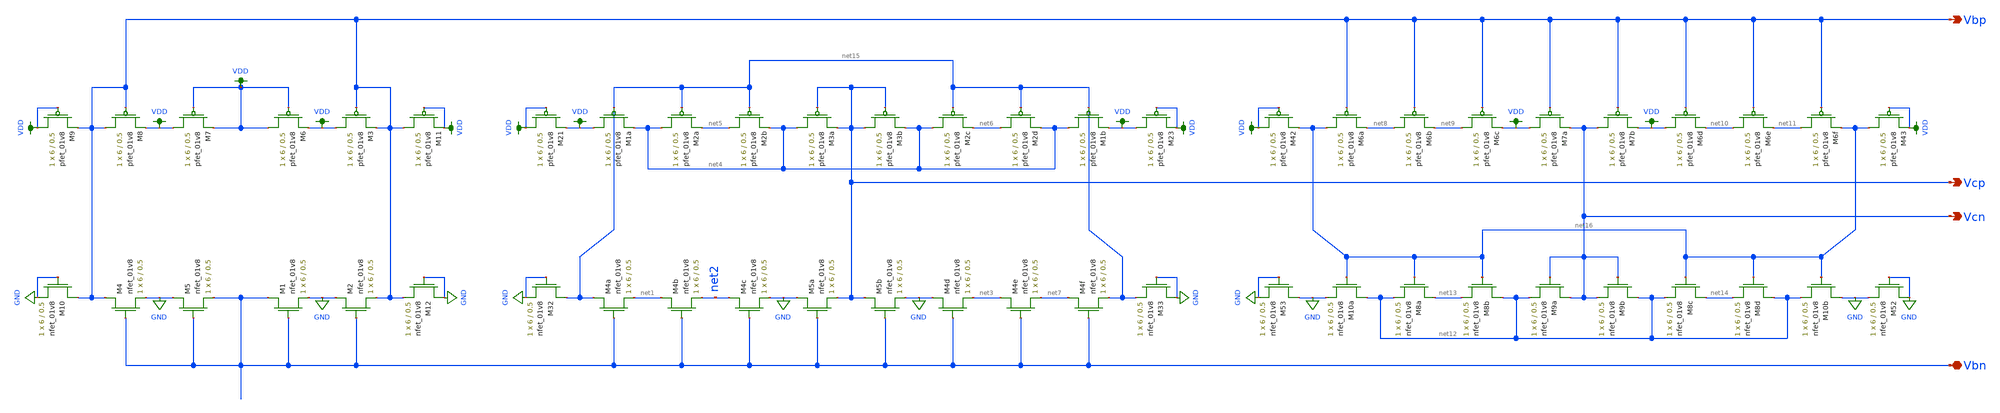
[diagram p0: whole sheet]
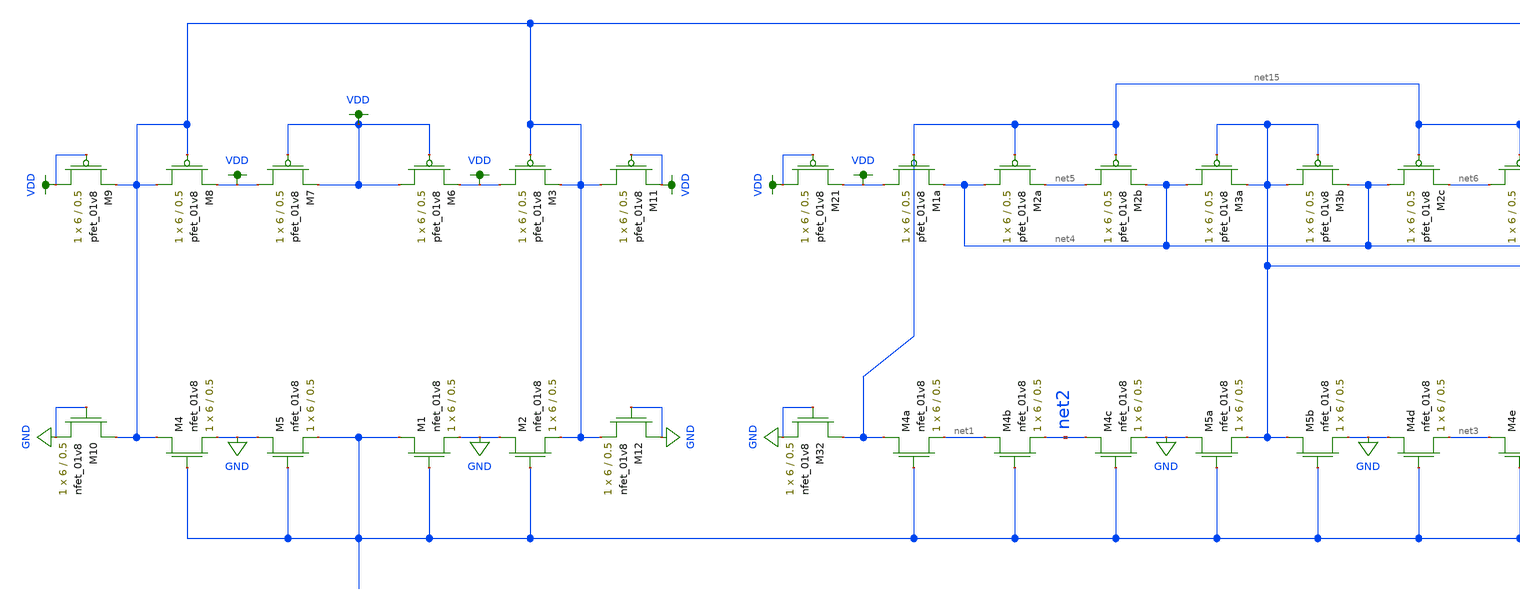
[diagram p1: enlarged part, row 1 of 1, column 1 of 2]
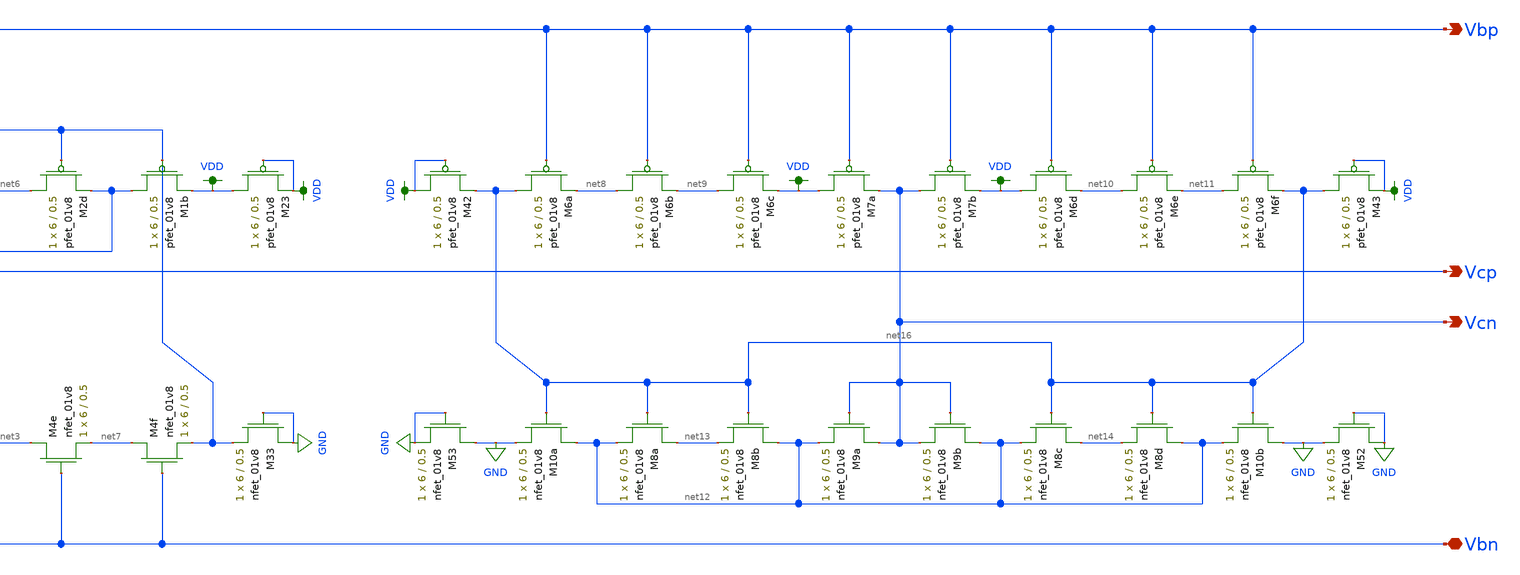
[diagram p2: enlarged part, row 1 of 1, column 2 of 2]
** sch_path: mini3/schem/bias_lvs.sch
**.subckt bias_lvs Vcn Vcp Vbp Vbn
*.opin Vcn
*.opin Vcp
*.opin Vbp
*.iopin Vbn
XM4a net15 Vbn net1 GND sky130_fd_pr__nfet_01v8 L=0.5 W=6 nf=1 ad='int((nf+1)/2) * W/nf * 0.29' as='int((nf+2)/2) * W/nf * 0.29'
+ pd='2*int((nf+1)/2) * (W/nf + 0.29)' ps='2*int((nf+2)/2) * (W/nf + 0.29)' nrd='0.29 / W' nrs='0.29 / W'
+ sa=0 sb=0 sd=0 mult=1 m=1
XM4b net1 Vbn net2 GND sky130_fd_pr__nfet_01v8 L=0.5 W=6 nf=1 ad='int((nf+1)/2) * W/nf * 0.29' as='int((nf+2)/2) * W/nf * 0.29'
+ pd='2*int((nf+1)/2) * (W/nf + 0.29)' ps='2*int((nf+2)/2) * (W/nf + 0.29)' nrd='0.29 / W' nrs='0.29 / W'
+ sa=0 sb=0 sd=0 mult=1 m=1
XM4c net2 Vbn GND GND sky130_fd_pr__nfet_01v8 L=0.5 W=6 nf=1 ad='int((nf+1)/2) * W/nf * 0.29' as='int((nf+2)/2) * W/nf * 0.29'
+ pd='2*int((nf+1)/2) * (W/nf + 0.29)' ps='2*int((nf+2)/2) * (W/nf + 0.29)' nrd='0.29 / W' nrs='0.29 / W'
+ sa=0 sb=0 sd=0 mult=1 m=1
XM5a GND Vbn Vcp GND sky130_fd_pr__nfet_01v8 L=0.5 W=6 nf=1 ad='int((nf+1)/2) * W/nf * 0.29' as='int((nf+2)/2) * W/nf * 0.29'
+ pd='2*int((nf+1)/2) * (W/nf + 0.29)' ps='2*int((nf+2)/2) * (W/nf + 0.29)' nrd='0.29 / W' nrs='0.29 / W'
+ sa=0 sb=0 sd=0 mult=1 m=1
XM5b Vcp Vbn GND GND sky130_fd_pr__nfet_01v8 L=0.5 W=6 nf=1 ad='int((nf+1)/2) * W/nf * 0.29' as='int((nf+2)/2) * W/nf * 0.29'
+ pd='2*int((nf+1)/2) * (W/nf + 0.29)' ps='2*int((nf+2)/2) * (W/nf + 0.29)' nrd='0.29 / W' nrs='0.29 / W'
+ sa=0 sb=0 sd=0 mult=1 m=1
XM4d GND Vbn net3 GND sky130_fd_pr__nfet_01v8 L=0.5 W=6 nf=1 ad='int((nf+1)/2) * W/nf * 0.29' as='int((nf+2)/2) * W/nf * 0.29'
+ pd='2*int((nf+1)/2) * (W/nf + 0.29)' ps='2*int((nf+2)/2) * (W/nf + 0.29)' nrd='0.29 / W' nrs='0.29 / W'
+ sa=0 sb=0 sd=0 mult=1 m=1
XM4e net3 Vbn net7 GND sky130_fd_pr__nfet_01v8 L=0.5 W=6 nf=1 ad='int((nf+1)/2) * W/nf * 0.29' as='int((nf+2)/2) * W/nf * 0.29'
+ pd='2*int((nf+1)/2) * (W/nf + 0.29)' ps='2*int((nf+2)/2) * (W/nf + 0.29)' nrd='0.29 / W' nrs='0.29 / W'
+ sa=0 sb=0 sd=0 mult=1 m=1
XM4f net7 Vbn net15 GND sky130_fd_pr__nfet_01v8 L=0.5 W=6 nf=1 ad='int((nf+1)/2) * W/nf * 0.29' as='int((nf+2)/2) * W/nf * 0.29'
+ pd='2*int((nf+1)/2) * (W/nf + 0.29)' ps='2*int((nf+2)/2) * (W/nf + 0.29)' nrd='0.29 / W' nrs='0.29 / W'
+ sa=0 sb=0 sd=0 mult=1 m=1
XM1a VDD net15 net4 VDD sky130_fd_pr__pfet_01v8 L=0.5 W=6 nf=1 ad='int((nf+1)/2) * W/nf * 0.29' as='int((nf+2)/2) * W/nf * 0.29'
+ pd='2*int((nf+1)/2) * (W/nf + 0.29)' ps='2*int((nf+2)/2) * (W/nf + 0.29)' nrd='0.29 / W' nrs='0.29 / W'
+ sa=0 sb=0 sd=0 mult=1 m=1
XM2a net4 net15 net5 VDD sky130_fd_pr__pfet_01v8 L=0.5 W=6 nf=1 ad='int((nf+1)/2) * W/nf * 0.29' as='int((nf+2)/2) * W/nf * 0.29'
+ pd='2*int((nf+1)/2) * (W/nf + 0.29)' ps='2*int((nf+2)/2) * (W/nf + 0.29)' nrd='0.29 / W' nrs='0.29 / W'
+ sa=0 sb=0 sd=0 mult=1 m=1
XM2b net5 net15 net4 VDD sky130_fd_pr__pfet_01v8 L=0.5 W=6 nf=1 ad='int((nf+1)/2) * W/nf * 0.29' as='int((nf+2)/2) * W/nf * 0.29'
+ pd='2*int((nf+1)/2) * (W/nf + 0.29)' ps='2*int((nf+2)/2) * (W/nf + 0.29)' nrd='0.29 / W' nrs='0.29 / W'
+ sa=0 sb=0 sd=0 mult=1 m=1
XM3a net4 Vcp Vcp VDD sky130_fd_pr__pfet_01v8 L=0.5 W=6 nf=1 ad='int((nf+1)/2) * W/nf * 0.29' as='int((nf+2)/2) * W/nf * 0.29'
+ pd='2*int((nf+1)/2) * (W/nf + 0.29)' ps='2*int((nf+2)/2) * (W/nf + 0.29)' nrd='0.29 / W' nrs='0.29 / W'
+ sa=0 sb=0 sd=0 mult=1 m=1
XM3b Vcp Vcp net4 VDD sky130_fd_pr__pfet_01v8 L=0.5 W=6 nf=1 ad='int((nf+1)/2) * W/nf * 0.29' as='int((nf+2)/2) * W/nf * 0.29'
+ pd='2*int((nf+1)/2) * (W/nf + 0.29)' ps='2*int((nf+2)/2) * (W/nf + 0.29)' nrd='0.29 / W' nrs='0.29 / W'
+ sa=0 sb=0 sd=0 mult=1 m=1
XM2c net4 net15 net6 VDD sky130_fd_pr__pfet_01v8 L=0.5 W=6 nf=1 ad='int((nf+1)/2) * W/nf * 0.29' as='int((nf+2)/2) * W/nf * 0.29'
+ pd='2*int((nf+1)/2) * (W/nf + 0.29)' ps='2*int((nf+2)/2) * (W/nf + 0.29)' nrd='0.29 / W' nrs='0.29 / W'
+ sa=0 sb=0 sd=0 mult=1 m=1
XM2d net6 net15 net4 VDD sky130_fd_pr__pfet_01v8 L=0.5 W=6 nf=1 ad='int((nf+1)/2) * W/nf * 0.29' as='int((nf+2)/2) * W/nf * 0.29'
+ pd='2*int((nf+1)/2) * (W/nf + 0.29)' ps='2*int((nf+2)/2) * (W/nf + 0.29)' nrd='0.29 / W' nrs='0.29 / W'
+ sa=0 sb=0 sd=0 mult=1 m=1
XM1b net4 net15 VDD VDD sky130_fd_pr__pfet_01v8 L=0.5 W=6 nf=1 ad='int((nf+1)/2) * W/nf * 0.29' as='int((nf+2)/2) * W/nf * 0.29'
+ pd='2*int((nf+1)/2) * (W/nf + 0.29)' ps='2*int((nf+2)/2) * (W/nf + 0.29)' nrd='0.29 / W' nrs='0.29 / W'
+ sa=0 sb=0 sd=0 mult=1 m=1
XM6a net16 Vbp net8 VDD sky130_fd_pr__pfet_01v8 L=0.5 W=6 nf=1 ad='int((nf+1)/2) * W/nf * 0.29' as='int((nf+2)/2) * W/nf * 0.29'
+ pd='2*int((nf+1)/2) * (W/nf + 0.29)' ps='2*int((nf+2)/2) * (W/nf + 0.29)' nrd='0.29 / W' nrs='0.29 / W'
+ sa=0 sb=0 sd=0 mult=1 m=1
XM6b net8 Vbp net9 VDD sky130_fd_pr__pfet_01v8 L=0.5 W=6 nf=1 ad='int((nf+1)/2) * W/nf * 0.29' as='int((nf+2)/2) * W/nf * 0.29'
+ pd='2*int((nf+1)/2) * (W/nf + 0.29)' ps='2*int((nf+2)/2) * (W/nf + 0.29)' nrd='0.29 / W' nrs='0.29 / W'
+ sa=0 sb=0 sd=0 mult=1 m=1
XM6c net9 Vbp VDD VDD sky130_fd_pr__pfet_01v8 L=0.5 W=6 nf=1 ad='int((nf+1)/2) * W/nf * 0.29' as='int((nf+2)/2) * W/nf * 0.29'
+ pd='2*int((nf+1)/2) * (W/nf + 0.29)' ps='2*int((nf+2)/2) * (W/nf + 0.29)' nrd='0.29 / W' nrs='0.29 / W'
+ sa=0 sb=0 sd=0 mult=1 m=1
XM7a VDD Vbp Vcn VDD sky130_fd_pr__pfet_01v8 L=0.5 W=6 nf=1 ad='int((nf+1)/2) * W/nf * 0.29' as='int((nf+2)/2) * W/nf * 0.29'
+ pd='2*int((nf+1)/2) * (W/nf + 0.29)' ps='2*int((nf+2)/2) * (W/nf + 0.29)' nrd='0.29 / W' nrs='0.29 / W'
+ sa=0 sb=0 sd=0 mult=1 m=1
XM7b Vcn Vbp VDD VDD sky130_fd_pr__pfet_01v8 L=0.5 W=6 nf=1 ad='int((nf+1)/2) * W/nf * 0.29' as='int((nf+2)/2) * W/nf * 0.29'
+ pd='2*int((nf+1)/2) * (W/nf + 0.29)' ps='2*int((nf+2)/2) * (W/nf + 0.29)' nrd='0.29 / W' nrs='0.29 / W'
+ sa=0 sb=0 sd=0 mult=1 m=1
XM6d VDD Vbp net10 VDD sky130_fd_pr__pfet_01v8 L=0.5 W=6 nf=1 ad='int((nf+1)/2) * W/nf * 0.29' as='int((nf+2)/2) * W/nf * 0.29'
+ pd='2*int((nf+1)/2) * (W/nf + 0.29)' ps='2*int((nf+2)/2) * (W/nf + 0.29)' nrd='0.29 / W' nrs='0.29 / W'
+ sa=0 sb=0 sd=0 mult=1 m=1
XM6e net10 Vbp net11 VDD sky130_fd_pr__pfet_01v8 L=0.5 W=6 nf=1 ad='int((nf+1)/2) * W/nf * 0.29' as='int((nf+2)/2) * W/nf * 0.29'
+ pd='2*int((nf+1)/2) * (W/nf + 0.29)' ps='2*int((nf+2)/2) * (W/nf + 0.29)' nrd='0.29 / W' nrs='0.29 / W'
+ sa=0 sb=0 sd=0 mult=1 m=1
XM6f net11 Vbp net16 VDD sky130_fd_pr__pfet_01v8 L=0.5 W=6 nf=1 ad='int((nf+1)/2) * W/nf * 0.29' as='int((nf+2)/2) * W/nf * 0.29'
+ pd='2*int((nf+1)/2) * (W/nf + 0.29)' ps='2*int((nf+2)/2) * (W/nf + 0.29)' nrd='0.29 / W' nrs='0.29 / W'
+ sa=0 sb=0 sd=0 mult=1 m=1
XM10a net12 net16 GND GND sky130_fd_pr__nfet_01v8 L=0.5 W=6 nf=1 ad='int((nf+1)/2) * W/nf * 0.29' as='int((nf+2)/2) * W/nf * 0.29'
+ pd='2*int((nf+1)/2) * (W/nf + 0.29)' ps='2*int((nf+2)/2) * (W/nf + 0.29)' nrd='0.29 / W' nrs='0.29 / W'
+ sa=0 sb=0 sd=0 mult=1 m=1
XM8a net13 net16 net12 GND sky130_fd_pr__nfet_01v8 L=0.5 W=6 nf=1 ad='int((nf+1)/2) * W/nf * 0.29' as='int((nf+2)/2) * W/nf * 0.29'
+ pd='2*int((nf+1)/2) * (W/nf + 0.29)' ps='2*int((nf+2)/2) * (W/nf + 0.29)' nrd='0.29 / W' nrs='0.29 / W'
+ sa=0 sb=0 sd=0 mult=1 m=1
XM8b net12 net16 net13 GND sky130_fd_pr__nfet_01v8 L=0.5 W=6 nf=1 ad='int((nf+1)/2) * W/nf * 0.29' as='int((nf+2)/2) * W/nf * 0.29'
+ pd='2*int((nf+1)/2) * (W/nf + 0.29)' ps='2*int((nf+2)/2) * (W/nf + 0.29)' nrd='0.29 / W' nrs='0.29 / W'
+ sa=0 sb=0 sd=0 mult=1 m=1
XM9a Vcn Vcn net12 GND sky130_fd_pr__nfet_01v8 L=0.5 W=6 nf=1 ad='int((nf+1)/2) * W/nf * 0.29' as='int((nf+2)/2) * W/nf * 0.29'
+ pd='2*int((nf+1)/2) * (W/nf + 0.29)' ps='2*int((nf+2)/2) * (W/nf + 0.29)' nrd='0.29 / W' nrs='0.29 / W'
+ sa=0 sb=0 sd=0 mult=1 m=1
XM9b net12 Vcn Vcn GND sky130_fd_pr__nfet_01v8 L=0.5 W=6 nf=1 ad='int((nf+1)/2) * W/nf * 0.29' as='int((nf+2)/2) * W/nf * 0.29'
+ pd='2*int((nf+1)/2) * (W/nf + 0.29)' ps='2*int((nf+2)/2) * (W/nf + 0.29)' nrd='0.29 / W' nrs='0.29 / W'
+ sa=0 sb=0 sd=0 mult=1 m=1
XM8c net14 net16 net12 GND sky130_fd_pr__nfet_01v8 L=0.5 W=6 nf=1 ad='int((nf+1)/2) * W/nf * 0.29' as='int((nf+2)/2) * W/nf * 0.29'
+ pd='2*int((nf+1)/2) * (W/nf + 0.29)' ps='2*int((nf+2)/2) * (W/nf + 0.29)' nrd='0.29 / W' nrs='0.29 / W'
+ sa=0 sb=0 sd=0 mult=1 m=1
XM8d net12 net16 net14 GND sky130_fd_pr__nfet_01v8 L=0.5 W=6 nf=1 ad='int((nf+1)/2) * W/nf * 0.29' as='int((nf+2)/2) * W/nf * 0.29'
+ pd='2*int((nf+1)/2) * (W/nf + 0.29)' ps='2*int((nf+2)/2) * (W/nf + 0.29)' nrd='0.29 / W' nrs='0.29 / W'
+ sa=0 sb=0 sd=0 mult=1 m=1
XM10b GND net16 net12 GND sky130_fd_pr__nfet_01v8 L=0.5 W=6 nf=1 ad='int((nf+1)/2) * W/nf * 0.29' as='int((nf+2)/2) * W/nf * 0.29'
+ pd='2*int((nf+1)/2) * (W/nf + 0.29)' ps='2*int((nf+2)/2) * (W/nf + 0.29)' nrd='0.29 / W' nrs='0.29 / W'
+ sa=0 sb=0 sd=0 mult=1 m=1
XM23 VDD VDD VDD VDD sky130_fd_pr__pfet_01v8 L=0.5 W=6 nf=1 ad='int((nf+1)/2) * W/nf * 0.29' as='int((nf+2)/2) * W/nf * 0.29'
+ pd='2*int((nf+1)/2) * (W/nf + 0.29)' ps='2*int((nf+2)/2) * (W/nf + 0.29)' nrd='0.29 / W' nrs='0.29 / W'
+ sa=0 sb=0 sd=0 mult=1 m=1
XM32 net15 GND GND GND sky130_fd_pr__nfet_01v8 L=0.5 W=6 nf=1 ad='int((nf+1)/2) * W/nf * 0.29' as='int((nf+2)/2) * W/nf * 0.29'
+ pd='2*int((nf+1)/2) * (W/nf + 0.29)' ps='2*int((nf+2)/2) * (W/nf + 0.29)' nrd='0.29 / W' nrs='0.29 / W'
+ sa=0 sb=0 sd=0 mult=1 m=1
XM33 GND GND net15 GND sky130_fd_pr__nfet_01v8 L=0.5 W=6 nf=1 ad='int((nf+1)/2) * W/nf * 0.29' as='int((nf+2)/2) * W/nf * 0.29'
+ pd='2*int((nf+1)/2) * (W/nf + 0.29)' ps='2*int((nf+2)/2) * (W/nf + 0.29)' nrd='0.29 / W' nrs='0.29 / W'
+ sa=0 sb=0 sd=0 mult=1 m=1
XM42 VDD VDD net16 VDD sky130_fd_pr__pfet_01v8 L=0.5 W=6 nf=1 ad='int((nf+1)/2) * W/nf * 0.29' as='int((nf+2)/2) * W/nf * 0.29'
+ pd='2*int((nf+1)/2) * (W/nf + 0.29)' ps='2*int((nf+2)/2) * (W/nf + 0.29)' nrd='0.29 / W' nrs='0.29 / W'
+ sa=0 sb=0 sd=0 mult=1 m=1
XM43 net16 VDD VDD VDD sky130_fd_pr__pfet_01v8 L=0.5 W=6 nf=1 ad='int((nf+1)/2) * W/nf * 0.29' as='int((nf+2)/2) * W/nf * 0.29'
+ pd='2*int((nf+1)/2) * (W/nf + 0.29)' ps='2*int((nf+2)/2) * (W/nf + 0.29)' nrd='0.29 / W' nrs='0.29 / W'
+ sa=0 sb=0 sd=0 mult=1 m=1
XM52 GND GND GND GND sky130_fd_pr__nfet_01v8 L=0.5 W=6 nf=1 ad='int((nf+1)/2) * W/nf * 0.29' as='int((nf+2)/2) * W/nf * 0.29'
+ pd='2*int((nf+1)/2) * (W/nf + 0.29)' ps='2*int((nf+2)/2) * (W/nf + 0.29)' nrd='0.29 / W' nrs='0.29 / W'
+ sa=0 sb=0 sd=0 mult=1 m=1
XM53 GND GND GND GND sky130_fd_pr__nfet_01v8 L=0.5 W=6 nf=1 ad='int((nf+1)/2) * W/nf * 0.29' as='int((nf+2)/2) * W/nf * 0.29'
+ pd='2*int((nf+1)/2) * (W/nf + 0.29)' ps='2*int((nf+2)/2) * (W/nf + 0.29)' nrd='0.29 / W' nrs='0.29 / W'
+ sa=0 sb=0 sd=0 mult=1 m=1
XM21 VDD VDD VDD VDD sky130_fd_pr__pfet_01v8 L=0.5 W=6 nf=1 ad='int((nf+1)/2) * W/nf * 0.29' as='int((nf+2)/2) * W/nf * 0.29'
+ pd='2*int((nf+1)/2) * (W/nf + 0.29)' ps='2*int((nf+2)/2) * (W/nf + 0.29)' nrd='0.29 / W' nrs='0.29 / W'
+ sa=0 sb=0 sd=0 mult=1 m=1
XM1 Vbn Vbn GND GND sky130_fd_pr__nfet_01v8 L=0.5 W=6 nf=1 ad='int((nf+1)/2) * W/nf * 0.29' as='int((nf+2)/2) * W/nf * 0.29'
+ pd='2*int((nf+1)/2) * (W/nf + 0.29)' ps='2*int((nf+2)/2) * (W/nf + 0.29)' nrd='0.29 / W' nrs='0.29 / W'
+ sa=0 sb=0 sd=0 mult=1 m=1
XM2 GND Vbn Vbp GND sky130_fd_pr__nfet_01v8 L=0.5 W=6 nf=1 ad='int((nf+1)/2) * W/nf * 0.29' as='int((nf+2)/2) * W/nf * 0.29'
+ pd='2*int((nf+1)/2) * (W/nf + 0.29)' ps='2*int((nf+2)/2) * (W/nf + 0.29)' nrd='0.29 / W' nrs='0.29 / W'
+ sa=0 sb=0 sd=0 mult=1 m=1
XM3 VDD Vbp Vbp VDD sky130_fd_pr__pfet_01v8 L=0.5 W=6 nf=1 ad='int((nf+1)/2) * W/nf * 0.29' as='int((nf+2)/2) * W/nf * 0.29'
+ pd='2*int((nf+1)/2) * (W/nf + 0.29)' ps='2*int((nf+2)/2) * (W/nf + 0.29)' nrd='0.29 / W' nrs='0.29 / W'
+ sa=0 sb=0 sd=0 mult=1 m=1
XM4 Vbp Vbn GND GND sky130_fd_pr__nfet_01v8 L=0.5 W=6 nf=1 ad='int((nf+1)/2) * W/nf * 0.29' as='int((nf+2)/2) * W/nf * 0.29'
+ pd='2*int((nf+1)/2) * (W/nf + 0.29)' ps='2*int((nf+2)/2) * (W/nf + 0.29)' nrd='0.29 / W' nrs='0.29 / W'
+ sa=0 sb=0 sd=0 mult=1 m=1
XM5 GND Vbn Vbn GND sky130_fd_pr__nfet_01v8 L=0.5 W=6 nf=1 ad='int((nf+1)/2) * W/nf * 0.29' as='int((nf+2)/2) * W/nf * 0.29'
+ pd='2*int((nf+1)/2) * (W/nf + 0.29)' ps='2*int((nf+2)/2) * (W/nf + 0.29)' nrd='0.29 / W' nrs='0.29 / W'
+ sa=0 sb=0 sd=0 mult=1 m=1
XM6 VDD VDD VDD VDD sky130_fd_pr__pfet_01v8 L=0.5 W=6 nf=1 ad='int((nf+1)/2) * W/nf * 0.29' as='int((nf+2)/2) * W/nf * 0.29'
+ pd='2*int((nf+1)/2) * (W/nf + 0.29)' ps='2*int((nf+2)/2) * (W/nf + 0.29)' nrd='0.29 / W' nrs='0.29 / W'
+ sa=0 sb=0 sd=0 mult=1 m=1
XM7 VDD VDD VDD VDD sky130_fd_pr__pfet_01v8 L=0.5 W=6 nf=1 ad='int((nf+1)/2) * W/nf * 0.29' as='int((nf+2)/2) * W/nf * 0.29'
+ pd='2*int((nf+1)/2) * (W/nf + 0.29)' ps='2*int((nf+2)/2) * (W/nf + 0.29)' nrd='0.29 / W' nrs='0.29 / W'
+ sa=0 sb=0 sd=0 mult=1 m=1
XM8 Vbp Vbp VDD VDD sky130_fd_pr__pfet_01v8 L=0.5 W=6 nf=1 ad='int((nf+1)/2) * W/nf * 0.29' as='int((nf+2)/2) * W/nf * 0.29'
+ pd='2*int((nf+1)/2) * (W/nf + 0.29)' ps='2*int((nf+2)/2) * (W/nf + 0.29)' nrd='0.29 / W' nrs='0.29 / W'
+ sa=0 sb=0 sd=0 mult=1 m=1
XM9 VDD VDD Vbp VDD sky130_fd_pr__pfet_01v8 L=0.5 W=6 nf=1 ad='int((nf+1)/2) * W/nf * 0.29' as='int((nf+2)/2) * W/nf * 0.29'
+ pd='2*int((nf+1)/2) * (W/nf + 0.29)' ps='2*int((nf+2)/2) * (W/nf + 0.29)' nrd='0.29 / W' nrs='0.29 / W'
+ sa=0 sb=0 sd=0 mult=1 m=1
XM10 Vbp GND GND GND sky130_fd_pr__nfet_01v8 L=0.5 W=6 nf=1 ad='int((nf+1)/2) * W/nf * 0.29' as='int((nf+2)/2) * W/nf * 0.29'
+ pd='2*int((nf+1)/2) * (W/nf + 0.29)' ps='2*int((nf+2)/2) * (W/nf + 0.29)' nrd='0.29 / W' nrs='0.29 / W'
+ sa=0 sb=0 sd=0 mult=1 m=1
XM11 Vbp VDD VDD VDD sky130_fd_pr__pfet_01v8 L=0.5 W=6 nf=1 ad='int((nf+1)/2) * W/nf * 0.29' as='int((nf+2)/2) * W/nf * 0.29'
+ pd='2*int((nf+1)/2) * (W/nf + 0.29)' ps='2*int((nf+2)/2) * (W/nf + 0.29)' nrd='0.29 / W' nrs='0.29 / W'
+ sa=0 sb=0 sd=0 mult=1 m=1
XM12 GND GND Vbp GND sky130_fd_pr__nfet_01v8 L=0.5 W=6 nf=1 ad='int((nf+1)/2) * W/nf * 0.29' as='int((nf+2)/2) * W/nf * 0.29'
+ pd='2*int((nf+1)/2) * (W/nf + 0.29)' ps='2*int((nf+2)/2) * (W/nf + 0.29)' nrd='0.29 / W' nrs='0.29 / W'
+ sa=0 sb=0 sd=0 mult=1 m=1
**.ends
.GLOBAL VDD
.GLOBAL GND
.end
